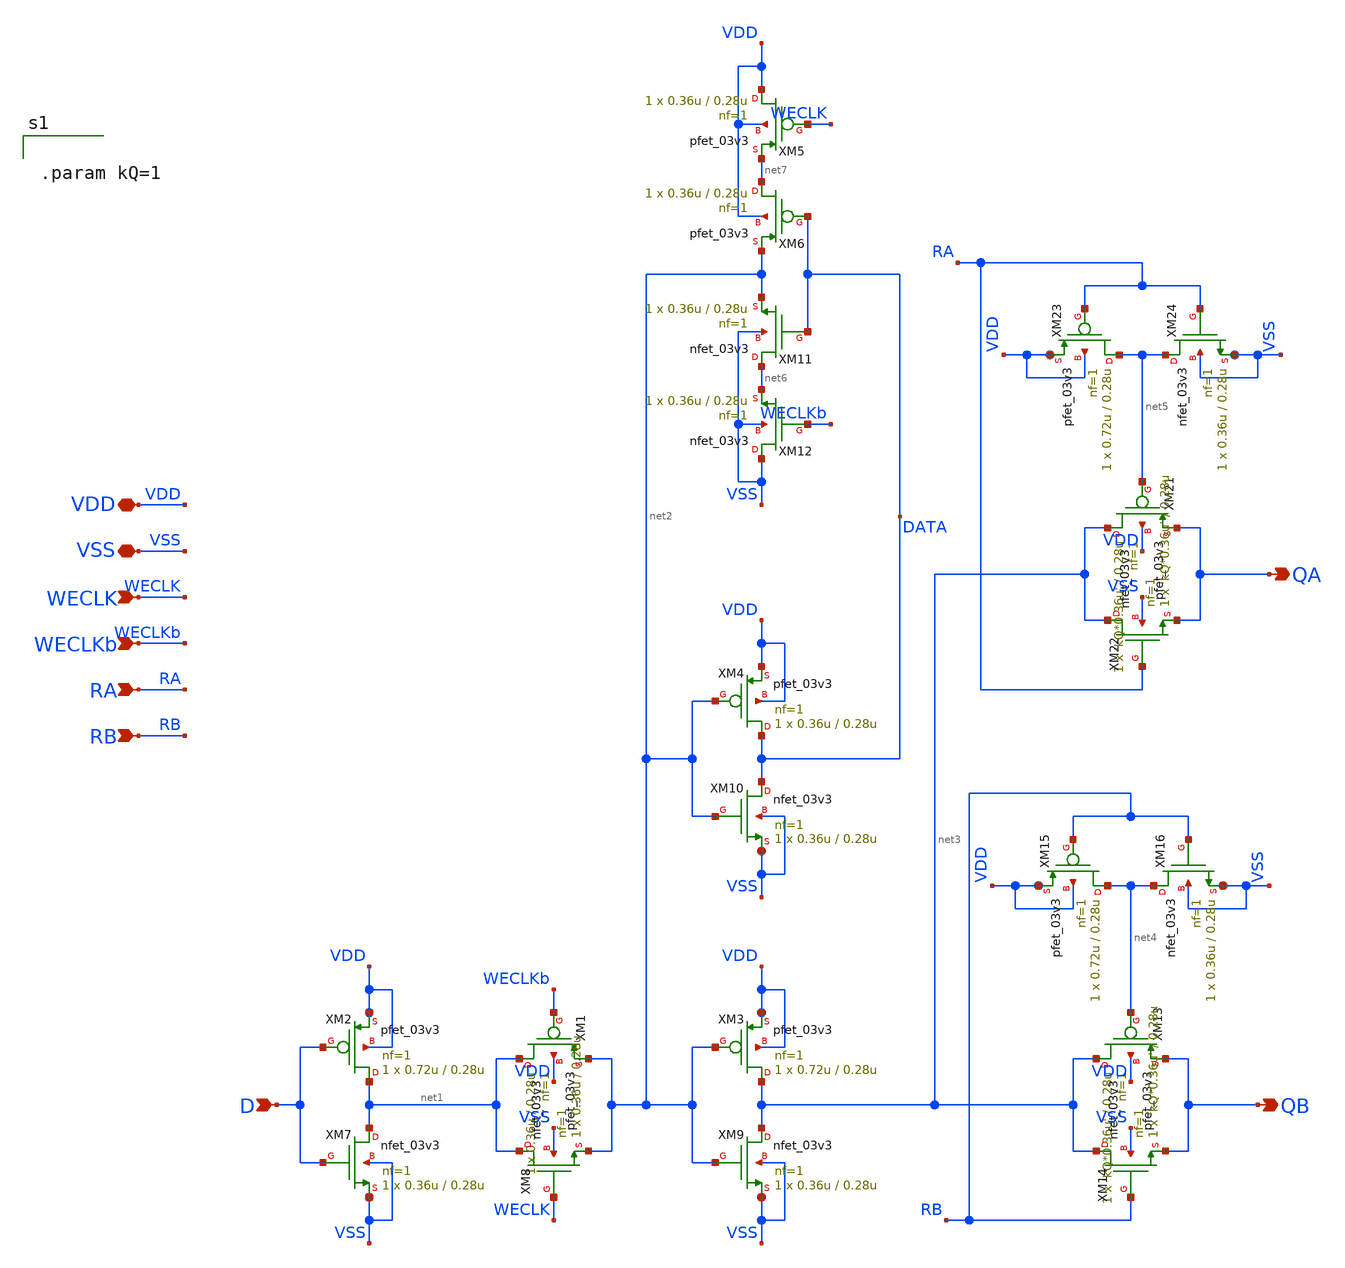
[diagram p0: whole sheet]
** sch_path: CAD3/slave_latch.sch
**.subckt slave_latch D RA RB WECLKb WECLK QA QB VDD VSS
*.ipin D
*.ipin RA
*.ipin RB
*.ipin WECLKb
*.ipin WECLK
*.opin QA
*.opin QB
*.iopin VDD
*.iopin VSS
XM1 net1 WECLKb net2 VDD pfet_03v3 L=0.28u W=0.36u nf=1 ad='int((nf+1)/2) * W/nf * 0.18u' as='int((nf+2)/2) * W/nf * 0.18u'
+ pd='2*int((nf+1)/2) * (W/nf + 0.18u)' ps='2*int((nf+2)/2) * (W/nf + 0.18u)' nrd='0.18u / W' nrs='0.18u / W'
+ sa=0 sb=0 sd=0 m=1
XM2 net1 D VDD VDD pfet_03v3 L=0.28u W=0.72u nf=1 ad='int((nf+1)/2) * W/nf * 0.18u' as='int((nf+2)/2) * W/nf * 0.18u'
+ pd='2*int((nf+1)/2) * (W/nf + 0.18u)' ps='2*int((nf+2)/2) * (W/nf + 0.18u)' nrd='0.18u / W' nrs='0.18u / W'
+ sa=0 sb=0 sd=0 m=1
XM3 net3 net2 VDD VDD pfet_03v3 L=0.28u W=0.72u nf=1 ad='int((nf+1)/2) * W/nf * 0.18u' as='int((nf+2)/2) * W/nf * 0.18u'
+ pd='2*int((nf+1)/2) * (W/nf + 0.18u)' ps='2*int((nf+2)/2) * (W/nf + 0.18u)' nrd='0.18u / W' nrs='0.18u / W'
+ sa=0 sb=0 sd=0 m=1
XM4 DATA net2 VDD VDD pfet_03v3 L=0.28u W=0.36u nf=1 ad='int((nf+1)/2) * W/nf * 0.18u' as='int((nf+2)/2) * W/nf * 0.18u'
+ pd='2*int((nf+1)/2) * (W/nf + 0.18u)' ps='2*int((nf+2)/2) * (W/nf + 0.18u)' nrd='0.18u / W' nrs='0.18u / W'
+ sa=0 sb=0 sd=0 m=1
XM5 VDD WECLK net7 VDD pfet_03v3 L=0.28u W=0.36u nf=1 ad='int((nf+1)/2) * W/nf * 0.18u' as='int((nf+2)/2) * W/nf * 0.18u'
+ pd='2*int((nf+1)/2) * (W/nf + 0.18u)' ps='2*int((nf+2)/2) * (W/nf + 0.18u)' nrd='0.18u / W' nrs='0.18u / W'
+ sa=0 sb=0 sd=0 m=1
XM6 net7 DATA net2 VDD pfet_03v3 L=0.28u W=0.36u nf=1 ad='int((nf+1)/2) * W/nf * 0.18u' as='int((nf+2)/2) * W/nf * 0.18u'
+ pd='2*int((nf+1)/2) * (W/nf + 0.18u)' ps='2*int((nf+2)/2) * (W/nf + 0.18u)' nrd='0.18u / W' nrs='0.18u / W'
+ sa=0 sb=0 sd=0 m=1
XM7 net1 D VSS VSS nfet_03v3 L=0.28u W=0.36u nf=1 ad='int((nf+1)/2) * W/nf * 0.18u' as='int((nf+2)/2) * W/nf * 0.18u'
+ pd='2*int((nf+1)/2) * (W/nf + 0.18u)' ps='2*int((nf+2)/2) * (W/nf + 0.18u)' nrd='0.18u / W' nrs='0.18u / W'
+ sa=0 sb=0 sd=0 m=1
XM8 net1 WECLK net2 VSS nfet_03v3 L=0.28u W=0.36u nf=1 ad='int((nf+1)/2) * W/nf * 0.18u' as='int((nf+2)/2) * W/nf * 0.18u'
+ pd='2*int((nf+1)/2) * (W/nf + 0.18u)' ps='2*int((nf+2)/2) * (W/nf + 0.18u)' nrd='0.18u / W' nrs='0.18u / W'
+ sa=0 sb=0 sd=0 m=1
XM9 net3 net2 VSS VSS nfet_03v3 L=0.28u W=0.36u nf=1 ad='int((nf+1)/2) * W/nf * 0.18u' as='int((nf+2)/2) * W/nf * 0.18u'
+ pd='2*int((nf+1)/2) * (W/nf + 0.18u)' ps='2*int((nf+2)/2) * (W/nf + 0.18u)' nrd='0.18u / W' nrs='0.18u / W'
+ sa=0 sb=0 sd=0 m=1
XM10 DATA net2 VSS VSS nfet_03v3 L=0.28u W=0.36u nf=1 ad='int((nf+1)/2) * W/nf * 0.18u' as='int((nf+2)/2) * W/nf * 0.18u'
+ pd='2*int((nf+1)/2) * (W/nf + 0.18u)' ps='2*int((nf+2)/2) * (W/nf + 0.18u)' nrd='0.18u / W' nrs='0.18u / W'
+ sa=0 sb=0 sd=0 m=1
XM11 net6 DATA net2 VSS nfet_03v3 L=0.28u W=0.36u nf=1 ad='int((nf+1)/2) * W/nf * 0.18u' as='int((nf+2)/2) * W/nf * 0.18u'
+ pd='2*int((nf+1)/2) * (W/nf + 0.18u)' ps='2*int((nf+2)/2) * (W/nf + 0.18u)' nrd='0.18u / W' nrs='0.18u / W'
+ sa=0 sb=0 sd=0 m=1
XM12 VSS WECLKb net6 VSS nfet_03v3 L=0.28u W=0.36u nf=1 ad='int((nf+1)/2) * W/nf * 0.18u' as='int((nf+2)/2) * W/nf * 0.18u'
+ pd='2*int((nf+1)/2) * (W/nf + 0.18u)' ps='2*int((nf+2)/2) * (W/nf + 0.18u)' nrd='0.18u / W' nrs='0.18u / W'
+ sa=0 sb=0 sd=0 m=1
XM13 net3 net4 QB VDD pfet_03v3 L=0.28u W='kQ*0.36u' nf=1 ad='int((nf+1)/2) * W/nf * 0.18u' as='int((nf+2)/2) * W/nf * 0.18u'
+ pd='2*int((nf+1)/2) * (W/nf + 0.18u)' ps='2*int((nf+2)/2) * (W/nf + 0.18u)' nrd='0.18u / W' nrs='0.18u / W'
+ sa=0 sb=0 sd=0 m=1
XM14 net3 RB QB VSS nfet_03v3 L=0.28u W='kQ*0.36u' nf=1 ad='int((nf+1)/2) * W/nf * 0.18u' as='int((nf+2)/2) * W/nf * 0.18u'
+ pd='2*int((nf+1)/2) * (W/nf + 0.18u)' ps='2*int((nf+2)/2) * (W/nf + 0.18u)' nrd='0.18u / W' nrs='0.18u / W'
+ sa=0 sb=0 sd=0 m=1
XM15 net4 RB VDD VDD pfet_03v3 L=0.28u W=0.72u nf=1 ad='int((nf+1)/2) * W/nf * 0.18u' as='int((nf+2)/2) * W/nf * 0.18u'
+ pd='2*int((nf+1)/2) * (W/nf + 0.18u)' ps='2*int((nf+2)/2) * (W/nf + 0.18u)' nrd='0.18u / W' nrs='0.18u / W'
+ sa=0 sb=0 sd=0 m=1
XM16 net4 RB VSS VSS nfet_03v3 L=0.28u W=0.36u nf=1 ad='int((nf+1)/2) * W/nf * 0.18u' as='int((nf+2)/2) * W/nf * 0.18u'
+ pd='2*int((nf+1)/2) * (W/nf + 0.18u)' ps='2*int((nf+2)/2) * (W/nf + 0.18u)' nrd='0.18u / W' nrs='0.18u / W'
+ sa=0 sb=0 sd=0 m=1
XM21 net3 net5 QA VDD pfet_03v3 L=0.28u W='kQ*0.36u' nf=1 ad='int((nf+1)/2) * W/nf * 0.18u' as='int((nf+2)/2) * W/nf * 0.18u'
+ pd='2*int((nf+1)/2) * (W/nf + 0.18u)' ps='2*int((nf+2)/2) * (W/nf + 0.18u)' nrd='0.18u / W' nrs='0.18u / W'
+ sa=0 sb=0 sd=0 m=1
XM22 net3 RA QA VSS nfet_03v3 L=0.28u W='kQ*0.36u' nf=1 ad='int((nf+1)/2) * W/nf * 0.18u' as='int((nf+2)/2) * W/nf * 0.18u'
+ pd='2*int((nf+1)/2) * (W/nf + 0.18u)' ps='2*int((nf+2)/2) * (W/nf + 0.18u)' nrd='0.18u / W' nrs='0.18u / W'
+ sa=0 sb=0 sd=0 m=1
XM23 net5 RA VDD VDD pfet_03v3 L=0.28u W=0.72u nf=1 ad='int((nf+1)/2) * W/nf * 0.18u' as='int((nf+2)/2) * W/nf * 0.18u'
+ pd='2*int((nf+1)/2) * (W/nf + 0.18u)' ps='2*int((nf+2)/2) * (W/nf + 0.18u)' nrd='0.18u / W' nrs='0.18u / W'
+ sa=0 sb=0 sd=0 m=1
XM24 net5 RA VSS VSS nfet_03v3 L=0.28u W=0.36u nf=1 ad='int((nf+1)/2) * W/nf * 0.18u' as='int((nf+2)/2) * W/nf * 0.18u'
+ pd='2*int((nf+1)/2) * (W/nf + 0.18u)' ps='2*int((nf+2)/2) * (W/nf + 0.18u)' nrd='0.18u / W' nrs='0.18u / W'
+ sa=0 sb=0 sd=0 m=1
**** begin user architecture code


.param kQ=1


**** end user architecture code
**.ends
.end
